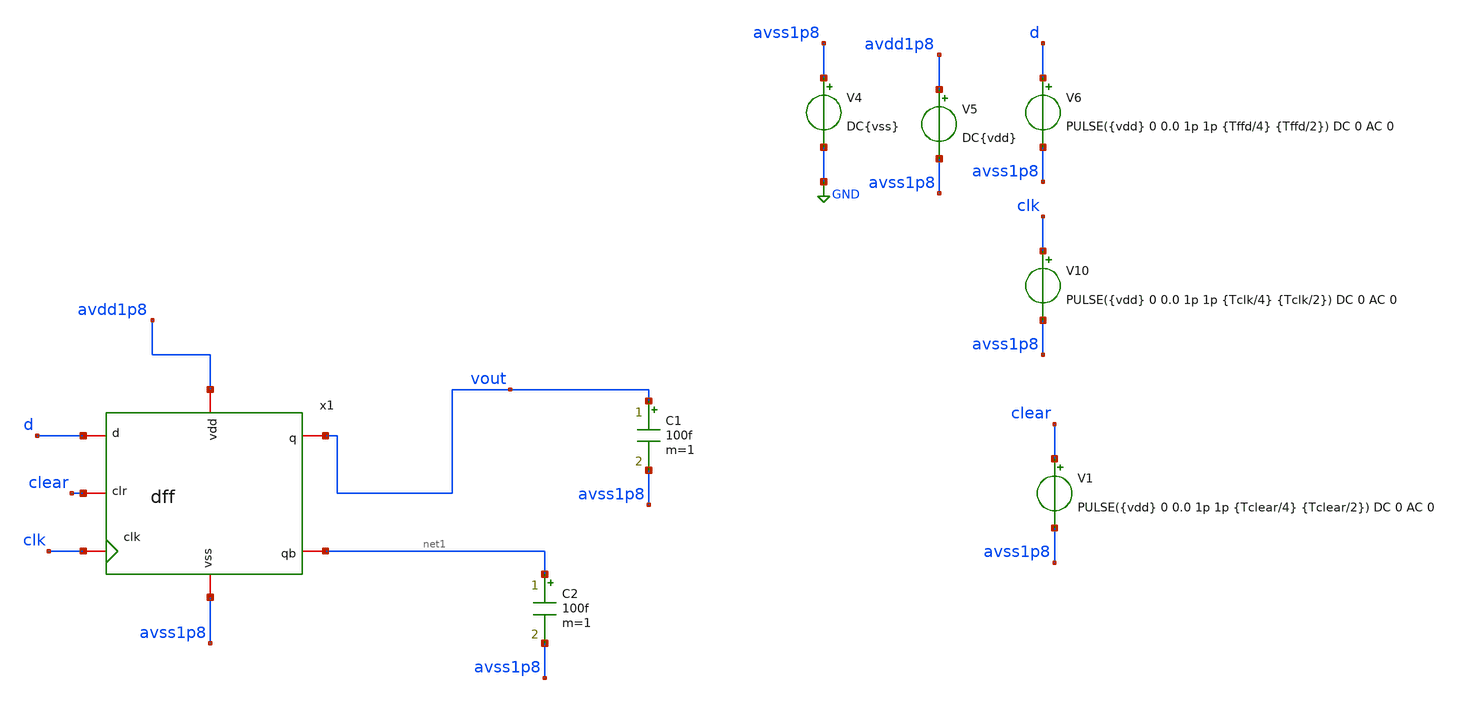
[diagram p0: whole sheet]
** sch_path: verification/testbenches/dff/tb_dff.sch
**.subckt tb_dff
x1 vout net1 d avss1p8 clk clear avdd1p8 dff
C1 vout avss1p8 100f m=1
V4 avss1p8 GND DC{vss}
V6 d avss1p8 PULSE({vdd} 0 0.0 1p 1p {Tffd/4} {Tffd/2}) DC 0 AC 0
V10 clk avss1p8 PULSE({vdd} 0 0.0 1p 1p {Tclk/4} {Tclk/2}) DC 0 AC 0
V5 avdd1p8 avss1p8 DC{vdd}
C2 net1 avss1p8 100f m=1
V1 clear avss1p8 PULSE({vdd} 0 0.0 1p 1p {Tclear/4} {Tclear/2}) DC 0 AC 0
**** begin user architecture code


* Circuit Parameters
.param vdd = 1.2
.param vss = 0.0
.param Tclk = 10n
.param Tffd = 85n
.param Tclear = 200n
.options TEMP = 27.0
* Include Models - IHP SG13G2
.lib cornerMOSlv.lib mos_tt
* OP Parameters & Singals to save
.save all
*Simulations
.control
tran 0.01u 300n
setplot tran1
plot v(d) v(clk)+1.2 v(clear)+2.4 v(vout)+3.6
reset
dc V6 0 1.2 0.01
setplot dc
plot vin vout ylabel vout xlabel vin
set filetype = ascii
write dcsweep.raw
.endc
.end


**** end user architecture code
**.ends

* expanding   symbol:  blocks/dff/schematic/dff.sym # of pins=7
** sym_path: design/blocks/dff/schematic/dff.sym
** sch_path: design/blocks/dff/schematic/dff.sch
.subckt dff q qb d vss clk clr vdd
*.iopin d
*.iopin clk
*.iopin clr
*.iopin q
*.iopin qb
*.iopin vdd
*.iopin vss
x1 clk vss net1 d vdd clkb transmissiongate
x2 vdd clr p1 net2 vss nor
x3 vdd clkb clk vss inverter
x4 clkb vss net1 net2 vdd clk transmissiongate
x5 clkb vss net3 p1 vdd clk transmissiongate
x6 clk vss qb net3 vdd clkb transmissiongate
x7 vdd clr net3 q vss nor
x8 vdd p1 net1 vss inverter
x9 vdd qb q vss inverter
.ends


* expanding   symbol:  blocks/transmissiongate/schematic/transmissiongate.sym # of pins=6
** sym_path: design/blocks/transmissiongate/schematic/transmissiongate.sym
** sch_path: design/blocks/transmissiongate/schematic/transmissiongate.sch
.subckt transmissiongate clk vss out d vdd clkb
*.iopin out
*.iopin d
*.iopin clkb
*.iopin clk
*.iopin vdd
*.iopin vss
XM1 out clkb d vdd sg13_lv_pmos w=1.5u l=0.15u ng=1 m=1 mm_ok=1
XM0 d clk out vss sg13_lv_nmos w=0.75u l=0.15u ng=1 m=1 mm_ok=1
.ends


* expanding   symbol:  blocks/norgate/schematic/nor.sym # of pins=5
** sym_path: design/blocks/norgate/schematic/nor.sym
** sch_path: design/blocks/norgate/schematic/nor.sch
.subckt nor vdd a b out vss
*.iopin vdd
*.iopin a
*.iopin vss
*.iopin out
*.iopin b
XM1 net1 a vdd vdd sg13_lv_pmos w=3.0u l=0.15u ng=1 m=1 mm_ok=1
XM2 out b vss vss sg13_lv_nmos w=0.75u l=0.15u ng=1 m=1 mm_ok=1
XM3 out a vss vss sg13_lv_nmos w=0.75u l=0.15u ng=1 m=1 mm_ok=1
XM4 out b net1 vdd sg13_lv_pmos w=3.0u l=0.15u ng=1 m=1 mm_ok=1
.ends


* expanding   symbol:  blocks/inverter/schematic/inverter.sym # of pins=4
** sym_path: design/blocks/inverter/schematic/inverter.sym
** sch_path: design/blocks/inverter/schematic/inverter.sch
.subckt inverter vdd out in vss
*.iopin vdd
*.iopin out
*.iopin vss
*.iopin in
XM1 out in vss vss sg13_lv_nmos w=0.75u l=0.15u ng=1 m=1 mm_ok=1
XM2 out in vdd vdd sg13_lv_pmos w=1.5u l=0.15u ng=1 m=1 mm_ok=1
.ends

.GLOBAL GND
.end
